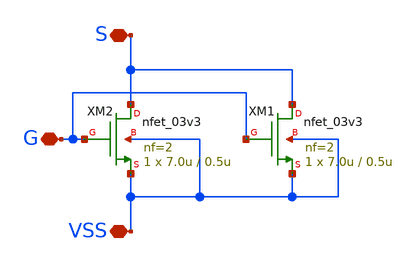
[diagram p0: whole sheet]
** sch_path: designs/libs/xp_core_analog/xp_play/PLAY.sch
**.subckt PLAY VSS G S
*.iopin VSS
*.iopin G
*.iopin S
XM2 S G VSS VSS nfet_03v3 L=0.5u W=7.0u nf=2 ad='int((nf+1)/2) * W/nf * 0.18u' as='int((nf+2)/2) * W/nf * 0.18u'
+ pd='2*int((nf+1)/2) * (W/nf + 0.18u)' ps='2*int((nf+2)/2) * (W/nf + 0.18u)' nrd='0.18u / W' nrs='0.18u / W'
+ sa=0 sb=0 sd=0 m=1
XM1 S G VSS VSS nfet_03v3 L=0.5u W=7.0u nf=2 ad='int((nf+1)/2) * W/nf * 0.18u' as='int((nf+2)/2) * W/nf * 0.18u'
+ pd='2*int((nf+1)/2) * (W/nf + 0.18u)' ps='2*int((nf+2)/2) * (W/nf + 0.18u)' nrd='0.18u / W' nrs='0.18u / W'
+ sa=0 sb=0 sd=0 m=1
**.ends
.end
